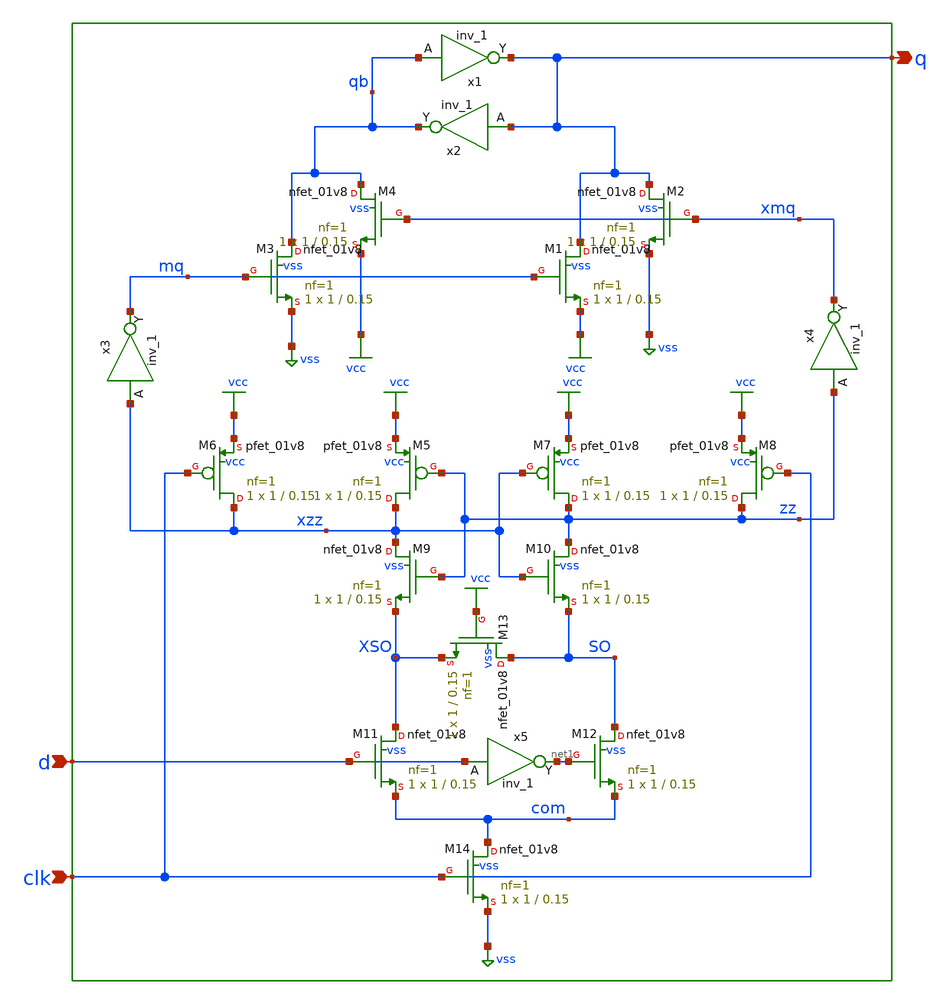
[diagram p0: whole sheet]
** sch_path: src/xe/test_cases/sa_latch.sch
**.subckt sa_latch clk q d
*.ipin clk
*.opin q
*.ipin d
x1 qb vss vss vcc vcc q sky130_fd_sc_hd__inv_1
x2 q vss vss vcc vcc qb sky130_fd_sc_hd__inv_1
XM3 qb mq vss vss sky130_fd_pr__nfet_01v8 L=0.15 W=1 nf=1 ad='int((nf+1)/2) * W/nf * 0.29' as='int((nf+2)/2) * W/nf * 0.29'
+ pd='2*int((nf+1)/2) * (W/nf + 0.29)' ps='2*int((nf+2)/2) * (W/nf + 0.29)' nrd='0.29 / W' nrs='0.29 / W'
+ sa=0 sb=0 sd=0 mult=1 m=1
XM4 qb xmq vcc vss sky130_fd_pr__nfet_01v8 L=0.15 W=1 nf=1 ad='int((nf+1)/2) * W/nf * 0.29' as='int((nf+2)/2) * W/nf * 0.29'
+ pd='2*int((nf+1)/2) * (W/nf + 0.29)' ps='2*int((nf+2)/2) * (W/nf + 0.29)' nrd='0.29 / W' nrs='0.29 / W'
+ sa=0 sb=0 sd=0 mult=1 m=1
XM1 q mq vcc vss sky130_fd_pr__nfet_01v8 L=0.15 W=1 nf=1 ad='int((nf+1)/2) * W/nf * 0.29' as='int((nf+2)/2) * W/nf * 0.29'
+ pd='2*int((nf+1)/2) * (W/nf + 0.29)' ps='2*int((nf+2)/2) * (W/nf + 0.29)' nrd='0.29 / W' nrs='0.29 / W'
+ sa=0 sb=0 sd=0 mult=1 m=1
XM2 q xmq vss vss sky130_fd_pr__nfet_01v8 L=0.15 W=1 nf=1 ad='int((nf+1)/2) * W/nf * 0.29' as='int((nf+2)/2) * W/nf * 0.29'
+ pd='2*int((nf+1)/2) * (W/nf + 0.29)' ps='2*int((nf+2)/2) * (W/nf + 0.29)' nrd='0.29 / W' nrs='0.29 / W'
+ sa=0 sb=0 sd=0 mult=1 m=1
x3 xzz vss vss vcc vcc mq sky130_fd_sc_hd__inv_1
x4 zz vss vss vcc vcc xmq sky130_fd_sc_hd__inv_1
XM5 xzz zz vcc vcc sky130_fd_pr__pfet_01v8 L=0.15 W=1 nf=1 ad='int((nf+1)/2) * W/nf * 0.29' as='int((nf+2)/2) * W/nf * 0.29'
+ pd='2*int((nf+1)/2) * (W/nf + 0.29)' ps='2*int((nf+2)/2) * (W/nf + 0.29)' nrd='0.29 / W' nrs='0.29 / W'
+ sa=0 sb=0 sd=0 mult=1 m=1
XM6 xzz clk vcc vcc sky130_fd_pr__pfet_01v8 L=0.15 W=1 nf=1 ad='int((nf+1)/2) * W/nf * 0.29' as='int((nf+2)/2) * W/nf * 0.29'
+ pd='2*int((nf+1)/2) * (W/nf + 0.29)' ps='2*int((nf+2)/2) * (W/nf + 0.29)' nrd='0.29 / W' nrs='0.29 / W'
+ sa=0 sb=0 sd=0 mult=1 m=1
XM7 zz xzz vcc vcc sky130_fd_pr__pfet_01v8 L=0.15 W=1 nf=1 ad='int((nf+1)/2) * W/nf * 0.29' as='int((nf+2)/2) * W/nf * 0.29'
+ pd='2*int((nf+1)/2) * (W/nf + 0.29)' ps='2*int((nf+2)/2) * (W/nf + 0.29)' nrd='0.29 / W' nrs='0.29 / W'
+ sa=0 sb=0 sd=0 mult=1 m=1
XM8 zz clk vcc vcc sky130_fd_pr__pfet_01v8 L=0.15 W=1 nf=1 ad='int((nf+1)/2) * W/nf * 0.29' as='int((nf+2)/2) * W/nf * 0.29'
+ pd='2*int((nf+1)/2) * (W/nf + 0.29)' ps='2*int((nf+2)/2) * (W/nf + 0.29)' nrd='0.29 / W' nrs='0.29 / W'
+ sa=0 sb=0 sd=0 mult=1 m=1
XM9 xzz zz XSO vss sky130_fd_pr__nfet_01v8 L=0.15 W=1 nf=1 ad='int((nf+1)/2) * W/nf * 0.29' as='int((nf+2)/2) * W/nf * 0.29'
+ pd='2*int((nf+1)/2) * (W/nf + 0.29)' ps='2*int((nf+2)/2) * (W/nf + 0.29)' nrd='0.29 / W' nrs='0.29 / W'
+ sa=0 sb=0 sd=0 mult=1 m=1
XM10 zz xzz SO vss sky130_fd_pr__nfet_01v8 L=0.15 W=1 nf=1 ad='int((nf+1)/2) * W/nf * 0.29' as='int((nf+2)/2) * W/nf * 0.29'
+ pd='2*int((nf+1)/2) * (W/nf + 0.29)' ps='2*int((nf+2)/2) * (W/nf + 0.29)' nrd='0.29 / W' nrs='0.29 / W'
+ sa=0 sb=0 sd=0 mult=1 m=1
XM11 XSO d com vss sky130_fd_pr__nfet_01v8 L=0.15 W=1 nf=1 ad='int((nf+1)/2) * W/nf * 0.29' as='int((nf+2)/2) * W/nf * 0.29'
+ pd='2*int((nf+1)/2) * (W/nf + 0.29)' ps='2*int((nf+2)/2) * (W/nf + 0.29)' nrd='0.29 / W' nrs='0.29 / W'
+ sa=0 sb=0 sd=0 mult=1 m=1
XM12 SO net1 com vss sky130_fd_pr__nfet_01v8 L=0.15 W=1 nf=1 ad='int((nf+1)/2) * W/nf * 0.29' as='int((nf+2)/2) * W/nf * 0.29'
+ pd='2*int((nf+1)/2) * (W/nf + 0.29)' ps='2*int((nf+2)/2) * (W/nf + 0.29)' nrd='0.29 / W' nrs='0.29 / W'
+ sa=0 sb=0 sd=0 mult=1 m=1
XM13 SO vcc XSO vss sky130_fd_pr__nfet_01v8 L=0.15 W=1 nf=1 ad='int((nf+1)/2) * W/nf * 0.29' as='int((nf+2)/2) * W/nf * 0.29'
+ pd='2*int((nf+1)/2) * (W/nf + 0.29)' ps='2*int((nf+2)/2) * (W/nf + 0.29)' nrd='0.29 / W' nrs='0.29 / W'
+ sa=0 sb=0 sd=0 mult=1 m=1
x5 d vss vss vcc vcc net1 sky130_fd_sc_hd__inv_1
XM14 com clk vss vss sky130_fd_pr__nfet_01v8 L=0.15 W=1 nf=1 ad='int((nf+1)/2) * W/nf * 0.29' as='int((nf+2)/2) * W/nf * 0.29'
+ pd='2*int((nf+1)/2) * (W/nf + 0.29)' ps='2*int((nf+2)/2) * (W/nf + 0.29)' nrd='0.29 / W' nrs='0.29 / W'
+ sa=0 sb=0 sd=0 mult=1 m=1
**.ends
.GLOBAL vcc
.GLOBAL vss
.end
